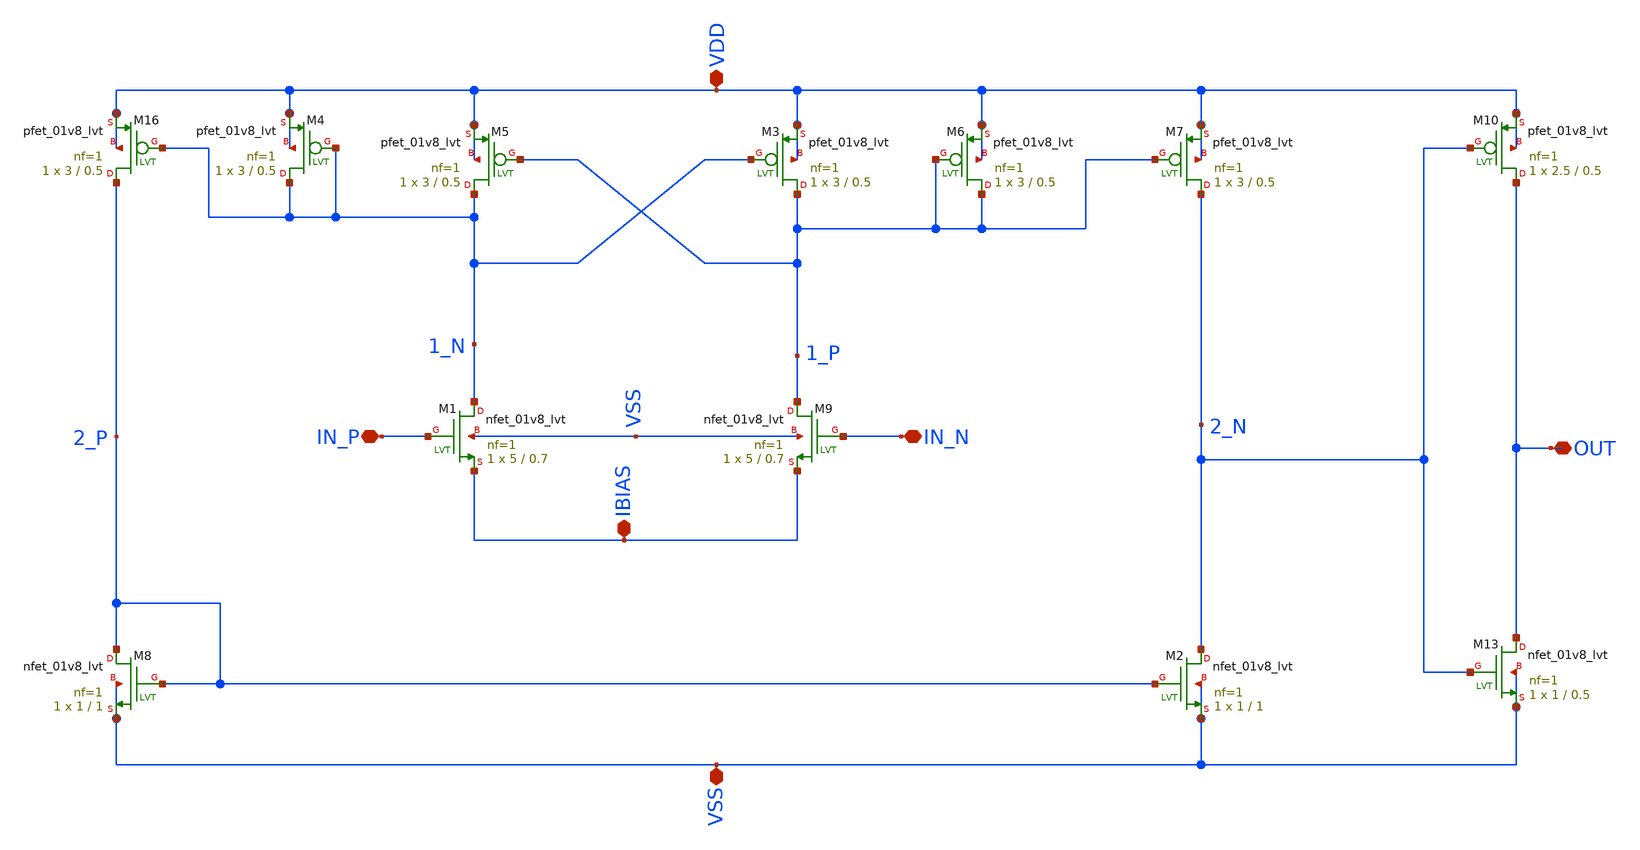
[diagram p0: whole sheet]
** sch_path: xschem/DC_DC_Converter_xschem/OTHERS/DC_DC_Converter_V7/Comparator/Comp_lvt.sch
**.subckt Comp_lvt VSS VDD IN_P IN_N OUT IBIAS
*.iopin VSS
*.iopin VDD
*.iopin IN_P
*.iopin IN_N
*.iopin OUT
*.iopin IBIAS
XM16 2_P 1_N VDD VDD sky130_fd_pr__pfet_01v8_lvt L=0.5 W=3 nf=1 ad='int((nf+1)/2) * W/nf * 0.29' as='int((nf+2)/2) * W/nf * 0.29'
+ pd='2*int((nf+1)/2) * (W/nf + 0.29)' ps='2*int((nf+2)/2) * (W/nf + 0.29)' nrd='0.29 / W' nrs='0.29 / W'
+ sa=0 sb=0 sd=0 mult=1 m=1
XM4 1_N 1_N VDD VDD sky130_fd_pr__pfet_01v8_lvt L=0.5 W=3 nf=1 ad='int((nf+1)/2) * W/nf * 0.29' as='int((nf+2)/2) * W/nf * 0.29'
+ pd='2*int((nf+1)/2) * (W/nf + 0.29)' ps='2*int((nf+2)/2) * (W/nf + 0.29)' nrd='0.29 / W' nrs='0.29 / W'
+ sa=0 sb=0 sd=0 mult=1 m=1
XM5 1_N 1_P VDD VDD sky130_fd_pr__pfet_01v8_lvt L=0.5 W=3 nf=1 ad='int((nf+1)/2) * W/nf * 0.29' as='int((nf+2)/2) * W/nf * 0.29'
+ pd='2*int((nf+1)/2) * (W/nf + 0.29)' ps='2*int((nf+2)/2) * (W/nf + 0.29)' nrd='0.29 / W' nrs='0.29 / W'
+ sa=0 sb=0 sd=0 mult=1 m=1
XM3 1_P 1_N VDD VDD sky130_fd_pr__pfet_01v8_lvt L=0.5 W=3 nf=1 ad='int((nf+1)/2) * W/nf * 0.29' as='int((nf+2)/2) * W/nf * 0.29'
+ pd='2*int((nf+1)/2) * (W/nf + 0.29)' ps='2*int((nf+2)/2) * (W/nf + 0.29)' nrd='0.29 / W' nrs='0.29 / W'
+ sa=0 sb=0 sd=0 mult=1 m=1
XM6 1_P 1_P VDD VDD sky130_fd_pr__pfet_01v8_lvt L=0.5 W=3 nf=1 ad='int((nf+1)/2) * W/nf * 0.29' as='int((nf+2)/2) * W/nf * 0.29'
+ pd='2*int((nf+1)/2) * (W/nf + 0.29)' ps='2*int((nf+2)/2) * (W/nf + 0.29)' nrd='0.29 / W' nrs='0.29 / W'
+ sa=0 sb=0 sd=0 mult=1 m=1
XM7 2_N 1_P VDD VDD sky130_fd_pr__pfet_01v8_lvt L=0.5 W=3 nf=1 ad='int((nf+1)/2) * W/nf * 0.29' as='int((nf+2)/2) * W/nf * 0.29'
+ pd='2*int((nf+1)/2) * (W/nf + 0.29)' ps='2*int((nf+2)/2) * (W/nf + 0.29)' nrd='0.29 / W' nrs='0.29 / W'
+ sa=0 sb=0 sd=0 mult=1 m=1
XM8 2_P 2_P VSS VSS sky130_fd_pr__nfet_01v8_lvt L=1 W=1 nf=1 ad='int((nf+1)/2) * W/nf * 0.29' as='int((nf+2)/2) * W/nf * 0.29'
+ pd='2*int((nf+1)/2) * (W/nf + 0.29)' ps='2*int((nf+2)/2) * (W/nf + 0.29)' nrd='0.29 / W' nrs='0.29 / W'
+ sa=0 sb=0 sd=0 mult=1 m=1
XM2 2_N 2_P VSS VSS sky130_fd_pr__nfet_01v8_lvt L=1 W=1 nf=1 ad='int((nf+1)/2) * W/nf * 0.29' as='int((nf+2)/2) * W/nf * 0.29'
+ pd='2*int((nf+1)/2) * (W/nf + 0.29)' ps='2*int((nf+2)/2) * (W/nf + 0.29)' nrd='0.29 / W' nrs='0.29 / W'
+ sa=0 sb=0 sd=0 mult=1 m=1
XM9 1_P IN_N IBIAS VSS sky130_fd_pr__nfet_01v8_lvt L=0.7 W=5 nf=1 ad='int((nf+1)/2) * W/nf * 0.29' as='int((nf+2)/2) * W/nf * 0.29'
+ pd='2*int((nf+1)/2) * (W/nf + 0.29)' ps='2*int((nf+2)/2) * (W/nf + 0.29)' nrd='0.29 / W' nrs='0.29 / W'
+ sa=0 sb=0 sd=0 mult=1 m=1
XM1 1_N IN_P IBIAS VSS sky130_fd_pr__nfet_01v8_lvt L=0.7 W=5 nf=1 ad='int((nf+1)/2) * W/nf * 0.29' as='int((nf+2)/2) * W/nf * 0.29'
+ pd='2*int((nf+1)/2) * (W/nf + 0.29)' ps='2*int((nf+2)/2) * (W/nf + 0.29)' nrd='0.29 / W' nrs='0.29 / W'
+ sa=0 sb=0 sd=0 mult=1 m=1
XM10 OUT 2_N VDD VDD sky130_fd_pr__pfet_01v8_lvt L=0.5 W=2.5 nf=1 ad='int((nf+1)/2) * W/nf * 0.29' as='int((nf+2)/2) * W/nf * 0.29'
+ pd='2*int((nf+1)/2) * (W/nf + 0.29)' ps='2*int((nf+2)/2) * (W/nf + 0.29)' nrd='0.29 / W' nrs='0.29 / W'
+ sa=0 sb=0 sd=0 mult=1 m=1
XM13 OUT 2_N VSS VSS sky130_fd_pr__nfet_01v8_lvt L=0.5 W=1 nf=1 ad='int((nf+1)/2) * W/nf * 0.29' as='int((nf+2)/2) * W/nf * 0.29'
+ pd='2*int((nf+1)/2) * (W/nf + 0.29)' ps='2*int((nf+2)/2) * (W/nf + 0.29)' nrd='0.29 / W' nrs='0.29 / W'
+ sa=0 sb=0 sd=0 mult=1 m=1
**.ends
.end
